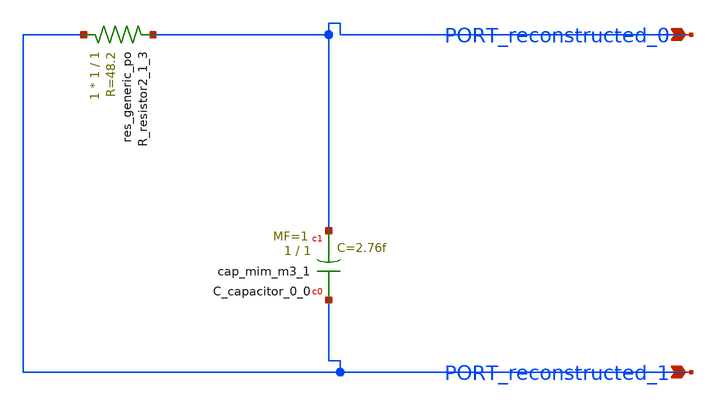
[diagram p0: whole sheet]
** sch_path: schematics/AMSNet/427.sch
**.subckt 427 PORT_reconstructed_1 PORT_reconstructed_0
*.ipin PORT_reconstructed_1
*.ipin PORT_reconstructed_0
XC_capacitor_0_0 PORT_reconstructed_1 PORT_reconstructed_0 sky130_fd_pr__cap_mim_m3_1 W=1 L=1 MF=1
+ m=1
XR_resistor2_1_3 PORT_reconstructed_1 PORT_reconstructed_0 sky130_fd_pr__res_generic_po W=1 L=1 m=1
**.ends
.end
